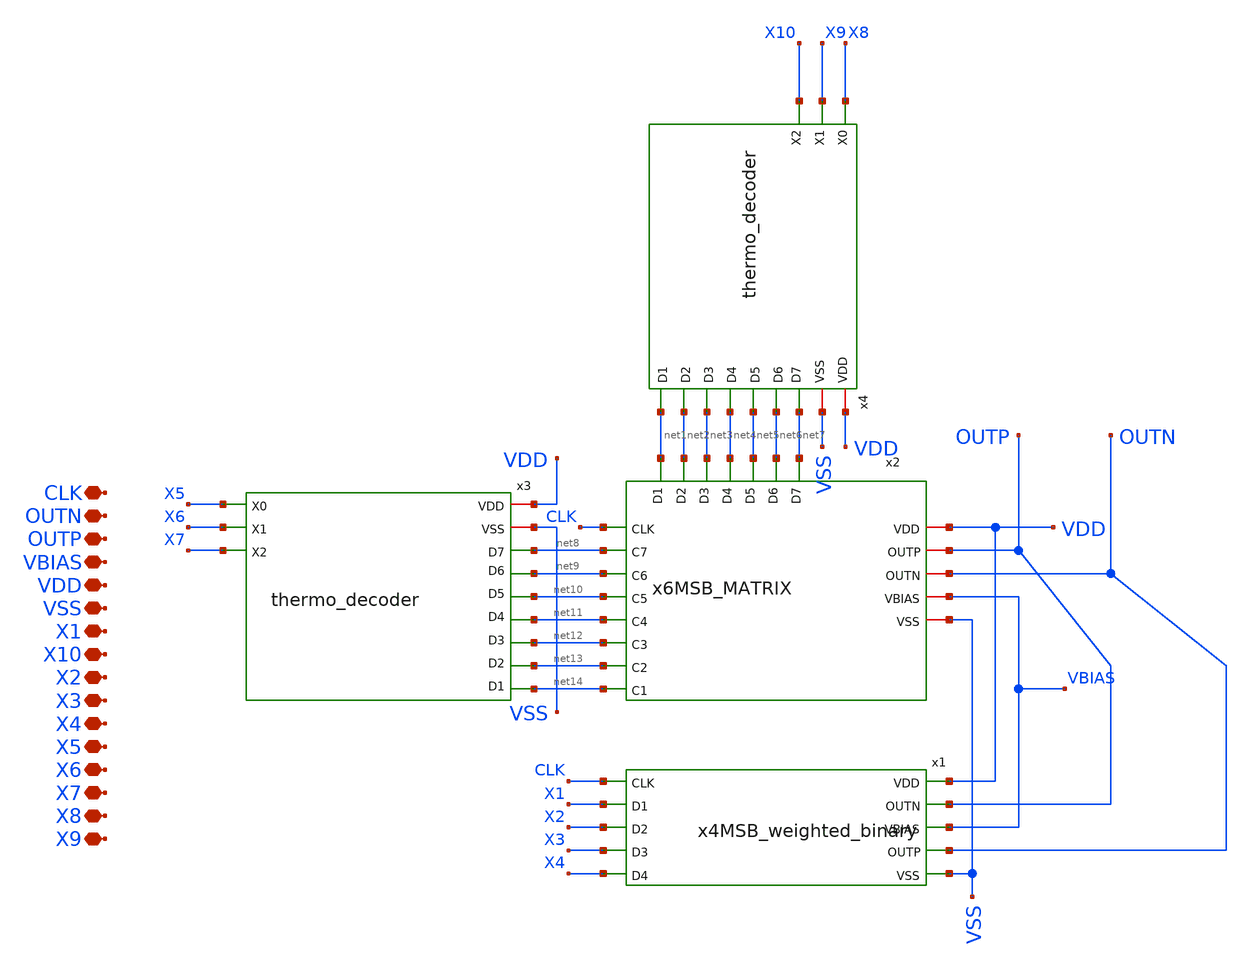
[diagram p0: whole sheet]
** sch_path: xschem/CS_DAC_10b.sch
**.subckt CS_DAC_10b X1 X2 X3 X4 X5 X6 X7 X8 X9 X10 CLK OUTP OUTN VBIAS VDD VSS
*.iopin X1
*.iopin X2
*.iopin X3
*.iopin X4
*.iopin X5
*.iopin X6
*.iopin X7
*.iopin X8
*.iopin X9
*.iopin X10
*.iopin CLK
*.iopin OUTP
*.iopin OUTN
*.iopin VBIAS
*.iopin VDD
*.iopin VSS
x3 X5 net10 net8 X7 net9 net13 X6 net11 net14 VSS VDD net12 thermo_decoder
x4 X8 net5 net7 X10 net6 net2 X9 net4 net1 VSS VDD net3 thermo_decoder
x1 X1 X2 X3 X4 OUTN OUTP CLK VBIAS VSS VDD x4MSB_weighted_binary
x2 net1 net2 net3 net4 net5 net6 net7 net14 net13 net12 net11 net10 net9 net8 CLK OUTP OUTN VBIAS
+ VSS VDD x6MSB_MATRIX
**.ends
.end
